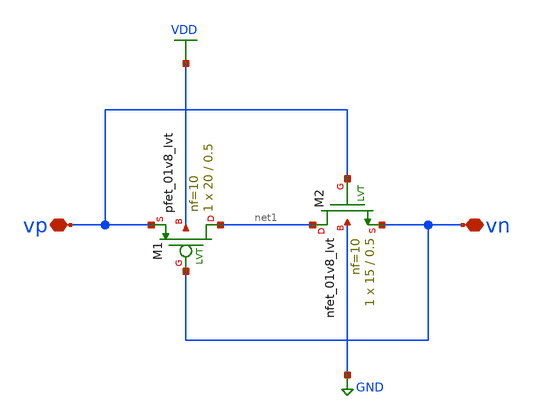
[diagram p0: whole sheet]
** sch_path: sample/ulpd/ulpd.sch
**.subckt ulpd vn vp
*.iopin vn
*.iopin vp
XM2 net1 vp vn GND sky130_fd_pr__nfet_01v8_lvt L=0.5 W=15 nf=10 ad='int((nf+1)/2) * W/nf * 0.29' as='int((nf+2)/2) * W/nf * 0.29'
+ pd='2*int((nf+1)/2) * (W/nf + 0.29)' ps='2*int((nf+2)/2) * (W/nf + 0.29)' nrd='0.29 / W' nrs='0.29 / W'
+ sa=0 sb=0 sd=0 mult=1 m=1
XM1 net1 vn vp VDD sky130_fd_pr__pfet_01v8_lvt L=0.5 W=20 nf=10 ad='int((nf+1)/2) * W/nf * 0.29' as='int((nf+2)/2) * W/nf * 0.29'
+ pd='2*int((nf+1)/2) * (W/nf + 0.29)' ps='2*int((nf+2)/2) * (W/nf + 0.29)' nrd='0.29 / W' nrs='0.29 / W'
+ sa=0 sb=0 sd=0 mult=1 m=1
**.ends
.GLOBAL VDD
.GLOBAL GND
.end
